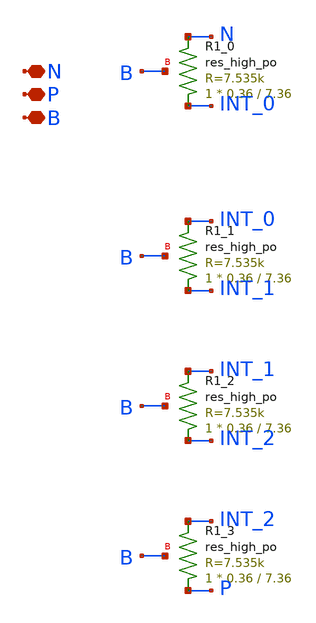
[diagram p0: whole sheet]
** sch_path: design/JNW_TR_SKY130A/JNWTR_RES4.sch
**.subckt JNWTR_RES4 N P B
*.iopin N
*.iopin P
*.iopin B
XR1_0 INT_0 N B sky130_fd_pr__res_high_po W=0.36 L=7.36 mult=1 m=1
XR1_1 INT_1 INT_0 B sky130_fd_pr__res_high_po W=0.36 L=7.36 mult=1 m=1
XR1_2 INT_2 INT_1 B sky130_fd_pr__res_high_po W=0.36 L=7.36 mult=1 m=1
XR1_3 P INT_2 B sky130_fd_pr__res_high_po W=0.36 L=7.36 mult=1 m=1
**.ends
.end
